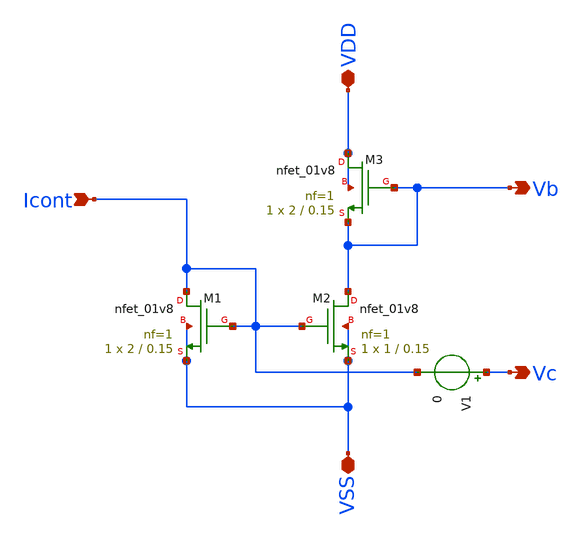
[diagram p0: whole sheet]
** sch_path: xschem/vco_bias.sch
**.subckt vco_bias VDD VSS Icont Vb Vc
*.iopin VDD
*.iopin VSS
*.ipin Icont
*.opin Vb
*.opin Vc
XM1 Icont Icont VSS VSS sky130_fd_pr__nfet_01v8 L=0.15 W=2 nf=1 ad='int((nf+1)/2) * W/nf * 0.29' as='int((nf+2)/2) * W/nf * 0.29'
+ pd='2*int((nf+1)/2) * (W/nf + 0.29)' ps='2*int((nf+2)/2) * (W/nf + 0.29)' nrd='0.29 / W' nrs='0.29 / W'
+ sa=0 sb=0 sd=0 mult=1 m=1
XM2 Vb Icont VSS VSS sky130_fd_pr__nfet_01v8 L=0.15 W=1 nf=1 ad='int((nf+1)/2) * W/nf * 0.29' as='int((nf+2)/2) * W/nf * 0.29'
+ pd='2*int((nf+1)/2) * (W/nf + 0.29)' ps='2*int((nf+2)/2) * (W/nf + 0.29)' nrd='0.29 / W' nrs='0.29 / W'
+ sa=0 sb=0 sd=0 mult=1 m=1
XM3 VDD Vb Vb VDD sky130_fd_pr__nfet_01v8 L=0.15 W=2 nf=1 ad='int((nf+1)/2) * W/nf * 0.29' as='int((nf+2)/2) * W/nf * 0.29'
+ pd='2*int((nf+1)/2) * (W/nf + 0.29)' ps='2*int((nf+2)/2) * (W/nf + 0.29)' nrd='0.29 / W' nrs='0.29 / W'
+ sa=0 sb=0 sd=0 mult=1 m=1
V1 Vc Icont 0
**.ends
.end
